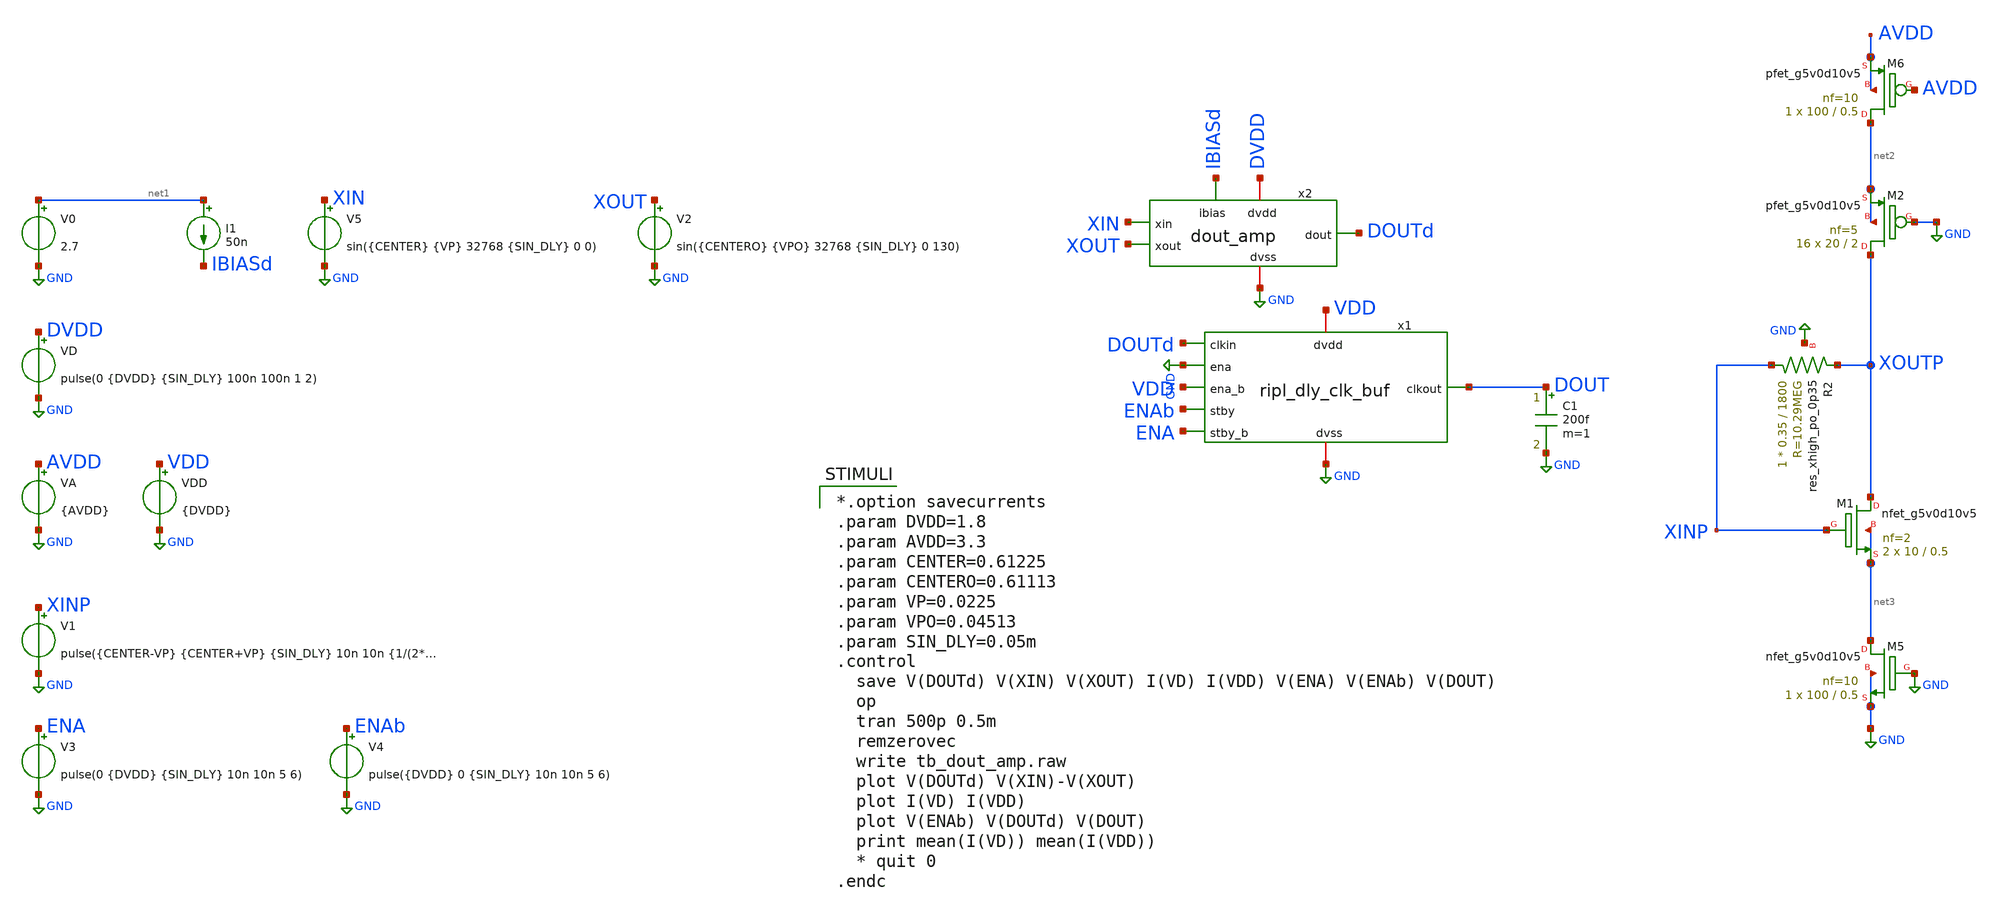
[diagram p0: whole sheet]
** sch_path: xschem/tb_dout_amp.sch
* xschem/dout_amp.sch:
* Copyright 2024 Brady Etz
* Licensed under the Apache License, Version 2.0 (the "License");

.lib $::SKYWATER_MODELS/sky130.lib.spice tt
.include $::SKYWATER_STDCELLS/sky130_fd_sc_hd.spice

**.subckt tb_dout_amp
VD DVDD GND pulse(0 {DVDD} {SIN_DLY} 100n 100n 1 2)
VA AVDD GND {AVDD}
V0 net1 GND 2.7
V5 XIN GND sin({CENTER} {VP} 32768 {SIN_DLY} 0 0)
V1 XINP GND pulse({CENTER-VP} {CENTER+VP} {SIN_DLY} 10n 10n {1/(2*32768)} {1/32768})
I1 net1 IBIASd 50n
V2 XOUT GND sin({CENTERO} {VPO} 32768 {SIN_DLY} 0 130)
C1 DOUT GND 200f m=1
XM1 XOUTP XINP net3 net3 sky130_fd_pr__nfet_g5v0d10v5 L=0.5 W=10 nf=2 ad='int((nf+1)/2) * W/nf * 0.29'
+ as='int((nf+2)/2) * W/nf * 0.29' pd='2*int((nf+1)/2) * (W/nf + 0.29)' ps='2*int((nf+2)/2) * (W/nf + 0.29)'
+ nrd='0.29 / W' nrs='0.29 / W' sa=0 sb=0 sd=0 mult=2 m=2
XM2 XOUTP GND net2 net2 sky130_fd_pr__pfet_g5v0d10v5 L=2 W=20 nf=5 ad='int((nf+1)/2) * W/nf * 0.29' as='int((nf+2)/2) * W/nf * 0.29'
+ pd='2*int((nf+1)/2) * (W/nf + 0.29)' ps='2*int((nf+2)/2) * (W/nf + 0.29)' nrd='0.29 / W' nrs='0.29 / W'
+ sa=0 sb=0 sd=0 mult=16 m=16
XR2 XINP XOUTP GND sky130_fd_pr__res_xhigh_po_0p35 L=1800 mult=1 m=1
XM5 net3 GND GND GND sky130_fd_pr__nfet_g5v0d10v5 L=0.5 W=100 nf=10 ad='int((nf+1)/2) * W/nf * 0.29'
+ as='int((nf+2)/2) * W/nf * 0.29' pd='2*int((nf+1)/2) * (W/nf + 0.29)' ps='2*int((nf+2)/2) * (W/nf + 0.29)'
+ nrd='0.29 / W' nrs='0.29 / W' sa=0 sb=0 sd=0 mult=1 m=1
XM6 net2 AVDD AVDD AVDD sky130_fd_pr__pfet_g5v0d10v5 L=0.5 W=100 nf=10 ad='int((nf+1)/2) * W/nf * 0.29'
+ as='int((nf+2)/2) * W/nf * 0.29' pd='2*int((nf+1)/2) * (W/nf + 0.29)' ps='2*int((nf+2)/2) * (W/nf + 0.29)'
+ nrd='0.29 / W' nrs='0.29 / W' sa=0 sb=0 sd=0 mult=1 m=1
V3 ENA GND pulse(0 {DVDD} {SIN_DLY} 10n 10n 5 6)
x1 VDD GND DOUTd DOUT GND VDD ENAb ENA ripl_dly_clk_buf
V4 ENAb GND pulse({DVDD} 0 {SIN_DLY} 10n 10n 5 6)
VDD VDD GND {DVDD}
x2 DVDD GND XIN XOUT IBIASd DOUTd dout_amp
**** begin user architecture code

*.option savecurrents
.param DVDD=1.8
.param AVDD=3.3
.param CENTER=0.61225
.param CENTERO=0.61113
.param VP=0.0225
.param VPO=0.04513
.param SIN_DLY=0.05m
.control
  save V(DOUTd) V(XIN) V(XOUT) I(VD) I(VDD) V(ENA) V(ENAb) V(DOUT)
  op
  tran 500p 0.5m
  remzerovec
  write tb_dout_amp.raw
  plot V(DOUTd) V(XIN)-V(XOUT)
  plot I(VD) I(VDD)
  plot V(ENAb) V(DOUTd) V(DOUT)
  print mean(I(VD)) mean(I(VDD))
  * quit 0
.endc

**** end user architecture code
**.ends

* expanding   symbol:  ripl_dly_clk_buf.sym # of pins=8
** sym_path: xschem/ripl_dly_clk_buf.sym
** sch_path: xschem/ripl_dly_clk_buf.sch
.subckt ripl_dly_clk_buf dvdd dvss clkin clkout ena ena_b stby stby_b
*.iopin dvdd
*.iopin dvss
*.ipin clkin
*.opin clkout
*.ipin ena
*.ipin stby
*.ipin ena_b
*.ipin stby_b
XM3 clkout clk_disable dvss dvss sky130_fd_pr__nfet_01v8 L=4 W=0.5 nf=1 ad='int((nf+1)/2) * W/nf * 0.29'
+ as='int((nf+2)/2) * W/nf * 0.29' pd='2*int((nf+1)/2) * (W/nf + 0.29)' ps='2*int((nf+2)/2) * (W/nf + 0.29)'
+ nrd='0.29 / W' nrs='0.29 / W' sa=0 sb=0 sd=0 mult=1 m=1
* noconn #net1
* noconn #net2
x3 ena ena_done_b stby_b stby_done_b stby dvss dvss dvdd dvdd clk_disable sky130_fd_sc_hd__a221o_1
x2 dvdd dvss clkin net2 stby_done_b stby_b ripple_dly_4
x1 dvdd dvss clkin net1 ena_done_b ena ripple_dly_4
x5 clkin clk_disable dvss dvss dvdd dvdd clkout sky130_fd_sc_hd__einvn_0
.ends


* expanding   symbol:  dout_amp.sym # of pins=6
** sym_path: xschem/dout_amp.sym
** sch_path: xschem/dout_amp.sch
.subckt dout_amp dvdd dvss xin xout ibias dout
*.ipin xin
*.iopin dvdd
*.iopin dvss
*.opin dout
*.ipin ibias
*.ipin xout
XM1 ibias ibias dvss dvss sky130_fd_pr__nfet_g5v0d10v5 L=2 W=2 nf=1 ad='int((nf+1)/2) * W/nf * 0.29'
+ as='int((nf+2)/2) * W/nf * 0.29' pd='2*int((nf+1)/2) * (W/nf + 0.29)' ps='2*int((nf+2)/2) * (W/nf + 0.29)'
+ nrd='0.29 / W' nrs='0.29 / W' sa=0 sb=0 sd=0 mult=5 m=5
XM2 vbp ibias dvss dvss sky130_fd_pr__nfet_g5v0d10v5 L=2 W=2 nf=1 ad='int((nf+1)/2) * W/nf * 0.29' as='int((nf+2)/2) * W/nf * 0.29'
+ pd='2*int((nf+1)/2) * (W/nf + 0.29)' ps='2*int((nf+2)/2) * (W/nf + 0.29)' nrd='0.29 / W' nrs='0.29 / W'
+ sa=0 sb=0 sd=0 mult=1 m=1
XM5 net2 xin tail dvdd sky130_fd_pr__pfet_g5v0d10v5 L=2 W=2 nf=1 ad='int((nf+1)/2) * W/nf * 0.29' as='int((nf+2)/2) * W/nf * 0.29'
+ pd='2*int((nf+1)/2) * (W/nf + 0.29)' ps='2*int((nf+2)/2) * (W/nf + 0.29)' nrd='0.29 / W' nrs='0.29 / W'
+ sa=0 sb=0 sd=0 mult=1 m=1
XC1 xin_buf inv_in sky130_fd_pr__cap_mim_m3_1 W=10 L=10 MF=12 m=12
XM6 inv_m1 inv_in dvdd dvdd sky130_fd_pr__pfet_01v8 L=8 W=0.5 nf=1 ad='int((nf+1)/2) * W/nf * 0.29' as='int((nf+2)/2) * W/nf * 0.29'
+ pd='2*int((nf+1)/2) * (W/nf + 0.29)' ps='2*int((nf+2)/2) * (W/nf + 0.29)' nrd='0.29 / W' nrs='0.29 / W'
+ sa=0 sb=0 sd=0 mult=1 m=1
XM7 inv_m1 inv_in dvss dvss sky130_fd_pr__nfet_01v8 L=8 W=0.5 nf=1 ad='int((nf+1)/2) * W/nf * 0.29' as='int((nf+2)/2) * W/nf * 0.29'
+ pd='2*int((nf+1)/2) * (W/nf + 0.29)' ps='2*int((nf+2)/2) * (W/nf + 0.29)' nrd='0.29 / W' nrs='0.29 / W'
+ sa=0 sb=0 sd=0 mult=1 m=1
XM8 net1 net1 dvdd dvdd sky130_fd_pr__pfet_01v8 L=8 W=0.5 nf=1 ad='int((nf+1)/2) * W/nf * 0.29' as='int((nf+2)/2) * W/nf * 0.29'
+ pd='2*int((nf+1)/2) * (W/nf + 0.29)' ps='2*int((nf+2)/2) * (W/nf + 0.29)' nrd='0.29 / W' nrs='0.29 / W'
+ sa=0 sb=0 sd=0 mult=1 m=1
XM9 net1 net1 dvss dvss sky130_fd_pr__nfet_01v8 L=8 W=0.5 nf=1 ad='int((nf+1)/2) * W/nf * 0.29' as='int((nf+2)/2) * W/nf * 0.29'
+ pd='2*int((nf+1)/2) * (W/nf + 0.29)' ps='2*int((nf+2)/2) * (W/nf + 0.29)' nrd='0.29 / W' nrs='0.29 / W'
+ sa=0 sb=0 sd=0 mult=1 m=1
XR1 inv_in net1 dvss sky130_fd_pr__res_xhigh_po_0p35 L=1000 mult=1 m=1
XM10 inv_m2 inv_m1 dvdd dvdd sky130_fd_pr__pfet_01v8 L=1 W=0.5 nf=1 ad='int((nf+1)/2) * W/nf * 0.29'
+ as='int((nf+2)/2) * W/nf * 0.29' pd='2*int((nf+1)/2) * (W/nf + 0.29)' ps='2*int((nf+2)/2) * (W/nf + 0.29)'
+ nrd='0.29 / W' nrs='0.29 / W' sa=0 sb=0 sd=0 mult=1 m=1
XM11 inv_m2 inv_m1 dvss dvss sky130_fd_pr__nfet_01v8 L=1 W=0.5 nf=1 ad='int((nf+1)/2) * W/nf * 0.29'
+ as='int((nf+2)/2) * W/nf * 0.29' pd='2*int((nf+1)/2) * (W/nf + 0.29)' ps='2*int((nf+2)/2) * (W/nf + 0.29)'
+ nrd='0.29 / W' nrs='0.29 / W' sa=0 sb=0 sd=0 mult=1 m=1
XM12 dout inv_m2 dvdd dvdd sky130_fd_pr__pfet_01v8 L=1 W=2 nf=1 ad='int((nf+1)/2) * W/nf * 0.29' as='int((nf+2)/2) * W/nf * 0.29'
+ pd='2*int((nf+1)/2) * (W/nf + 0.29)' ps='2*int((nf+2)/2) * (W/nf + 0.29)' nrd='0.29 / W' nrs='0.29 / W'
+ sa=0 sb=0 sd=0 mult=1 m=1
XM13 dout inv_m2 dvss dvss sky130_fd_pr__nfet_01v8 L=1 W=2 nf=1 ad='int((nf+1)/2) * W/nf * 0.29' as='int((nf+2)/2) * W/nf * 0.29'
+ pd='2*int((nf+1)/2) * (W/nf + 0.29)' ps='2*int((nf+2)/2) * (W/nf + 0.29)' nrd='0.29 / W' nrs='0.29 / W'
+ sa=0 sb=0 sd=0 mult=1 m=1
XM16 tail vbp dvdd dvdd sky130_fd_pr__pfet_01v8 L=2 W=4 nf=1 ad='int((nf+1)/2) * W/nf * 0.29' as='int((nf+2)/2) * W/nf * 0.29'
+ pd='2*int((nf+1)/2) * (W/nf + 0.29)' ps='2*int((nf+2)/2) * (W/nf + 0.29)' nrd='0.29 / W' nrs='0.29 / W'
+ sa=0 sb=0 sd=0 mult=5 m=5
XM17 vbp vbp dvdd dvdd sky130_fd_pr__pfet_01v8 L=2 W=2 nf=1 ad='int((nf+1)/2) * W/nf * 0.29' as='int((nf+2)/2) * W/nf * 0.29'
+ pd='2*int((nf+1)/2) * (W/nf + 0.29)' ps='2*int((nf+2)/2) * (W/nf + 0.29)' nrd='0.29 / W' nrs='0.29 / W'
+ sa=0 sb=0 sd=0 mult=1 m=1
XM3 xin_buf xout tail dvdd sky130_fd_pr__pfet_g5v0d10v5 L=2 W=2 nf=1 ad='int((nf+1)/2) * W/nf * 0.29'
+ as='int((nf+2)/2) * W/nf * 0.29' pd='2*int((nf+1)/2) * (W/nf + 0.29)' ps='2*int((nf+2)/2) * (W/nf + 0.29)'
+ nrd='0.29 / W' nrs='0.29 / W' sa=0 sb=0 sd=0 mult=1 m=1
XM4 xin_buf net2 dvss dvss sky130_fd_pr__nfet_01v8 L=2 W=4 nf=1 ad='int((nf+1)/2) * W/nf * 0.29' as='int((nf+2)/2) * W/nf * 0.29'
+ pd='2*int((nf+1)/2) * (W/nf + 0.29)' ps='2*int((nf+2)/2) * (W/nf + 0.29)' nrd='0.29 / W' nrs='0.29 / W'
+ sa=0 sb=0 sd=0 mult=1 m=1
XM18 net2 net2 dvss dvss sky130_fd_pr__nfet_01v8 L=2 W=4 nf=1 ad='int((nf+1)/2) * W/nf * 0.29' as='int((nf+2)/2) * W/nf * 0.29'
+ pd='2*int((nf+1)/2) * (W/nf + 0.29)' ps='2*int((nf+2)/2) * (W/nf + 0.29)' nrd='0.29 / W' nrs='0.29 / W'
+ sa=0 sb=0 sd=0 mult=1 m=1
.ends


* expanding   symbol:  ripple_dly_4.sym # of pins=6
** sym_path: xschem/ripple_dly_4.sym
** sch_path: xschem/ripple_dly_4.sch
.subckt ripple_dly_4 dvdd dvss clkin done doneb ena
*.ipin clkin
*.ipin ena
*.opin done
*.opin doneb
*.iopin dvdd
*.iopin dvss
x2 gated_clk Qb1 ena dvss dvss dvdd dvdd net1 Qb1 sky130_fd_sc_hd__dfrbp_1
x3 Qb1 Qb2 ena dvss dvss dvdd dvdd net2 Qb2 sky130_fd_sc_hd__dfrbp_1
* noconn #net1
* noconn #net2
x4 Qb2 doneb ena dvss dvss dvdd dvdd done doneb sky130_fd_sc_hd__dfrbp_1
x1 clkin doneb dvss dvss dvdd dvdd gated_clk sky130_fd_sc_hd__and2_0
.ends

.GLOBAL GND
.end
